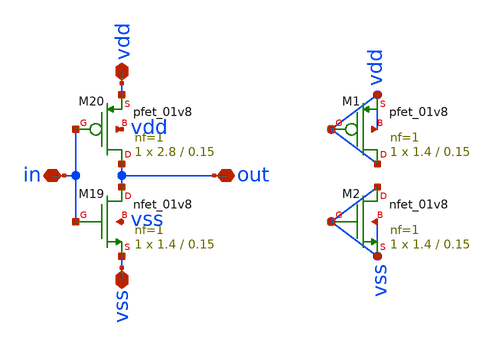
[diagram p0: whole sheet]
** sch_path: xschem/inv_simple1.sch
**.subckt inv_simple1 in vdd vss out
*.iopin in
*.iopin vdd
*.iopin vss
*.iopin out
XM19 out in vss vss sky130_fd_pr__nfet_01v8 L=0.15 W=1.4 nf=1 ad='int((nf+1)/2) * W/nf * 0.29' as='int((nf+2)/2) * W/nf * 0.29'
+ pd='2*int((nf+1)/2) * (W/nf + 0.29)' ps='2*int((nf+2)/2) * (W/nf + 0.29)' nrd='0.29 / W' nrs='0.29 / W'
+ sa=0 sb=0 sd=0 mult=1 m=1
XM20 out in vdd vdd sky130_fd_pr__pfet_01v8 L=0.15 W=2.8 nf=1 ad='int((nf+1)/2) * W/nf * 0.29' as='int((nf+2)/2) * W/nf * 0.29'
+ pd='2*int((nf+1)/2) * (W/nf + 0.29)' ps='2*int((nf+2)/2) * (W/nf + 0.29)' nrd='0.29 / W' nrs='0.29 / W'
+ sa=0 sb=0 sd=0 mult=1 m=1
XM1 vdd vdd vdd vdd sky130_fd_pr__pfet_01v8 L=0.15 W=1.4 nf=1 ad='int((nf+1)/2) * W/nf * 0.29' as='int((nf+2)/2) * W/nf * 0.29'
+ pd='2*int((nf+1)/2) * (W/nf + 0.29)' ps='2*int((nf+2)/2) * (W/nf + 0.29)' nrd='0.29 / W' nrs='0.29 / W'
+ sa=0 sb=0 sd=0 mult=1 m=1
XM2 vss vss vss vss sky130_fd_pr__nfet_01v8 L=0.15 W=1.4 nf=1 ad='int((nf+1)/2) * W/nf * 0.29' as='int((nf+2)/2) * W/nf * 0.29'
+ pd='2*int((nf+1)/2) * (W/nf + 0.29)' ps='2*int((nf+2)/2) * (W/nf + 0.29)' nrd='0.29 / W' nrs='0.29 / W'
+ sa=0 sb=0 sd=0 mult=1 m=1
**.ends
.end
